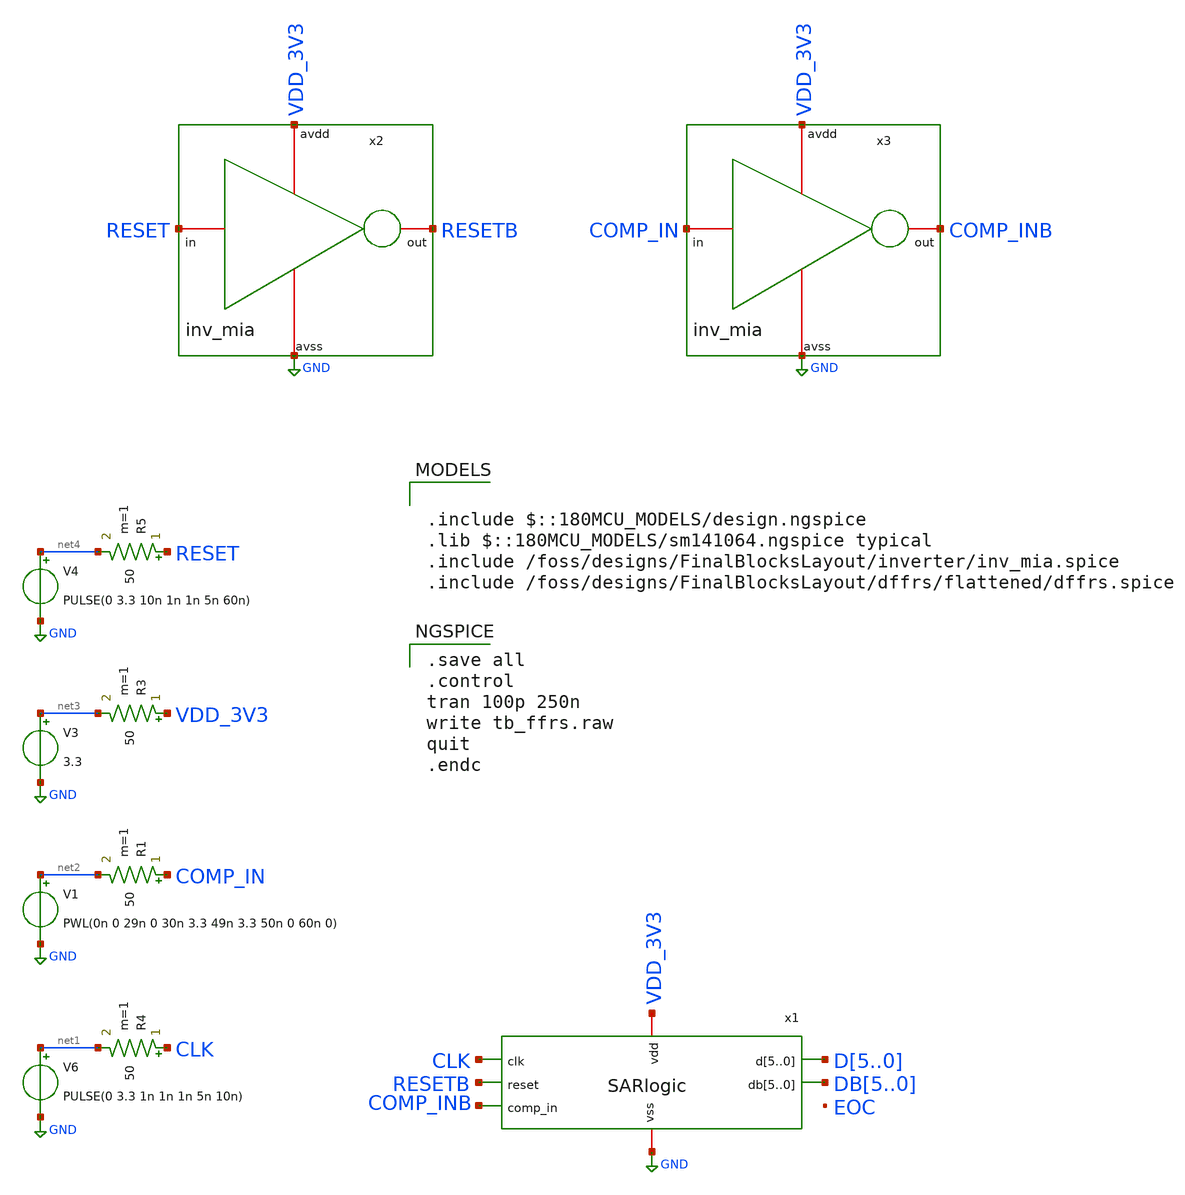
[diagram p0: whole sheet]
** sch_path: designs/FinalBlocksLayout/SARlogic/SAR_logic_tb.sch
**.subckt SAR_logic_tb
V6 net1 GND PULSE(0 3.3 1n 1n 1n 5n 10n)
R4 CLK net1 50 m=1
V1 net2 GND PWL(0n 0 29n 0 30n 3.3 49n 3.3 50n 0 60n 0)
R1 COMP_IN net2 50 m=1
V3 net3 GND 3.3
R3 VDD_3V3 net3 50 m=1
V4 net4 GND PULSE(0 3.3 10n 1n 1n 5n 60n)
R5 RESET net4 50 m=1
x2 VDD_3V3 RESET RESETB GND inv_mia
x3 VDD_3V3 COMP_IN COMP_INB GND inv_mia
x1 VDD_3V3 GND CLK RESETB COMP_INB D5 D4 D3 D2 D1 D0 DB5 DB4 DB3 DB2 DB1 DB0 SARlogic
**** begin user architecture code

.include $::180MCU_MODELS/design.ngspice
.lib $::180MCU_MODELS/sm141064.ngspice typical
.include /foss/designs/FinalBlocksLayout/inverter/inv_mia.spice
.include /foss/designs/FinalBlocksLayout/dffrs/flattened/dffrs.spice


.save all
.control
tran 100p 250n
write tb_ffrs.raw
quit
.endc

**** end user architecture code
**.ends

* expanding   symbol:  FinalBlocksLayout/SARlogic/SARlogic.sym # of pins=7
** sym_path: designs/FinalBlocksLayout/SARlogic/SARlogic.sym
** sch_path: designs/FinalBlocksLayout/SARlogic/SARlogic.sch
.subckt SARlogic vdd vss clk reset comp_in d5 d4 d3 d2 d1 d0 db5 db4 db3 db2 db1 db0
*.ipin comp_in
*.iopin vdd
*.iopin vss
*.ipin clk
*.ipin reset
*.opin d5,d4,d3,d2,d1,d0
*.opin db5,db4,db3,db2,db1,db0
x1 vdd vss vss clk reset vdd net1 net7 dffrs
x2 vdd vss net1 clk vdd reset net2 net8 dffrs
x3 vdd vss net2 clk vdd reset net3 net9 dffrs
x4 vdd vss net3 clk vdd reset net4 net10 dffrs
x5 vdd vss net4 clk vdd reset net5 net11 dffrs
x6 vdd vss net5 clk vdd reset net6 net12 dffrs
x7 vdd vss net6 clk vdd reset net15 net13 dffrs
x8 vdd vss comp_in d4 net7 reset d5 db5 dffrs
x9 vdd vss comp_in d3 net8 reset d4 db4 dffrs
x10 vdd vss comp_in d2 net9 reset d3 db3 dffrs
x11 vdd vss comp_in d1 net10 reset d2 db2 dffrs
x12 vdd vss comp_in d0 net11 reset d1 db1 dffrs
x13 vdd vss comp_in net14 net12 reset d0 db0 dffrs
x14 vdd vss vss vss net13 reset net14 net16 dffrs
.ends

.GLOBAL GND
.end
